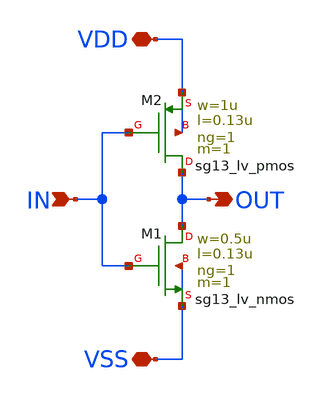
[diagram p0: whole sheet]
** sch_path: SSDOR_1.2V_v2/components/mux_ibias/mux2_b_inverter/mux2_b_inverter.sch
**.subckt mux2_b_inverter IN OUT VSS VDD
*.ipin IN
*.opin OUT
*.iopin VSS
*.iopin VDD
XM1 OUT IN VSS VSS sg13_lv_nmos w=0.5u l=0.13u ng=1 m=1 mm_ok=1
XM2 OUT IN VDD VDD sg13_lv_pmos w=1u l=0.13u ng=1 m=1 mm_ok=1
**.ends
.end
